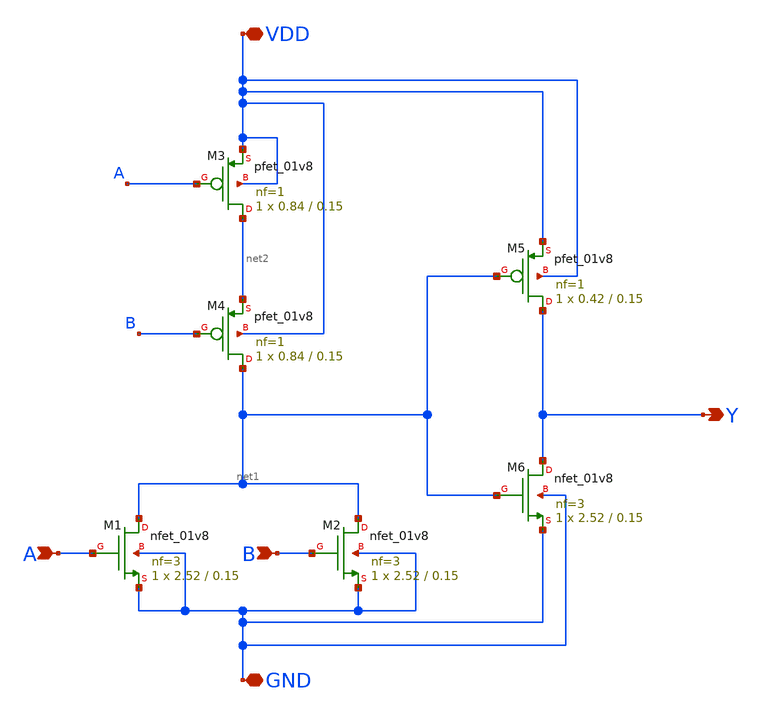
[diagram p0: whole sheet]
** sch_path: cells/OR2X1/schematic/or2x1.sch
**.subckt or2x1 A B VDD GND Y
*.ipin A
*.ipin B
*.iopin VDD
*.iopin GND
*.opin Y
XM1 net1 A GND GND sky130_fd_pr__nfet_01v8 L=0.15 W=2.52 nf=3 ad='int((3 + 1)/2) * 2.52 / 3 * 0.29' as='int((3 + 2)/2) * 2.52 / 3 * 0.29'
+ pd='2*int((3 + 1)/2) * (2.52 / 3 + 0.29)' ps='2*int((3 + 2)/2) * (2.52 / 3 + 0.29)' nrd='0.29 / 2.52 '
+ nrs='0.29 / 2.52 ' sa=0 sb=0 sd=0 mult=1 m=1
XM3 net2 A VDD VDD sky130_fd_pr__pfet_01v8 L=0.15 W=0.84 nf=1 ad='int((1 + 1)/2) * 0.84 / 1 * 0.29' as='int((1 + 2)/2) * 0.84 / 1 * 0.29'
+ pd='2*int((1 + 1)/2) * (0.84 / 1 + 0.29)' ps='2*int((1 + 2)/2) * (0.84 / 1 + 0.29)' nrd='0.29 / 0.84 '
+ nrs='0.29 / 0.84 ' sa=0 sb=0 sd=0 mult=1 m=1
XM5 Y net1 VDD VDD sky130_fd_pr__pfet_01v8 L=0.15 W=0.42 nf=1 ad='int((1 + 1)/2) * 0.42 / 1 * 0.29' as='int((1 + 2)/2) * 0.42 / 1 * 0.29'
+ pd='2*int((1 + 1)/2) * (0.42 / 1 + 0.29)' ps='2*int((1 + 2)/2) * (0.42 / 1 + 0.29)' nrd='0.29 / 0.42 '
+ nrs='0.29 / 0.42 ' sa=0 sb=0 sd=0 mult=1 m=1
XM4 net1 B net2 VDD sky130_fd_pr__pfet_01v8 L=0.15 W=0.84 nf=1 ad='int((1 + 1)/2) * 0.84 / 1 * 0.29'
+ as='int((1 + 2)/2) * 0.84 / 1 * 0.29' pd='2*int((1 + 1)/2) * (0.84 / 1 + 0.29)' ps='2*int((1 + 2)/2) * (0.84 / 1 + 0.29)'
+ nrd='0.29 / 0.84 ' nrs='0.29 / 0.84 ' sa=0 sb=0 sd=0 mult=1 m=1
XM2 net1 B GND GND sky130_fd_pr__nfet_01v8 L=0.15 W=2.52 nf=3 ad='int((3 + 1)/2) * 2.52 / 3 * 0.29' as='int((3 + 2)/2) * 2.52 / 3 * 0.29'
+ pd='2*int((3 + 1)/2) * (2.52 / 3 + 0.29)' ps='2*int((3 + 2)/2) * (2.52 / 3 + 0.29)' nrd='0.29 / 2.52 '
+ nrs='0.29 / 2.52 ' sa=0 sb=0 sd=0 mult=1 m=1
XM6 Y net1 GND GND sky130_fd_pr__nfet_01v8 L=0.15 W=2.52 nf=3 ad='int((3 + 1)/2) * 2.52 / 3 * 0.29' as='int((3 + 2)/2) * 2.52 / 3 * 0.29'
+ pd='2*int((3 + 1)/2) * (2.52 / 3 + 0.29)' ps='2*int((3 + 2)/2) * (2.52 / 3 + 0.29)' nrd='0.29 / 2.52 '
+ nrs='0.29 / 2.52 ' sa=0 sb=0 sd=0 mult=1 m=1
**.ends
.end
